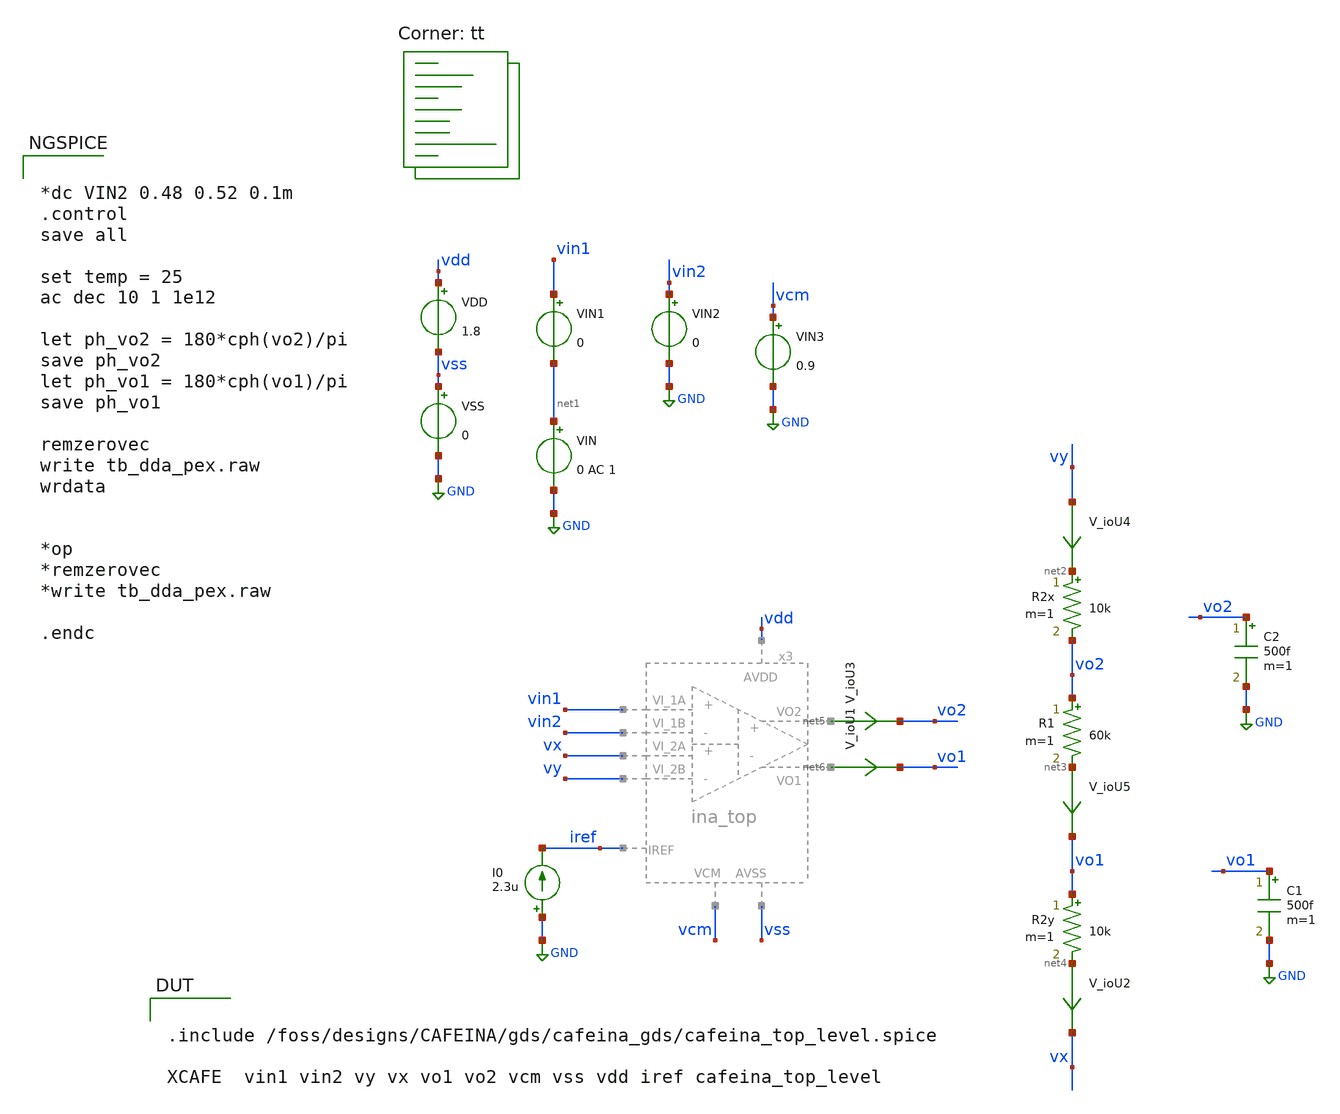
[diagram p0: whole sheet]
** sch_path: xschem/testbenches/tb_dda_pex.sch
**.subckt tb_dda_pex
VDD vdd vss 1.8
VSS vss GND 0
C1 vo1 GND 500f m=1
I0 GND iref 2.3u
VIN1 vin1 net1 0
VIN2 vin2 GND 0
VIN net1 GND 0 AC 1
C2 vo2 GND 500f m=1
VIN3 vcm GND 0.9
R2x net2 vo2 10k m=1
R1 vo2 net3 60k m=1
R2y vo1 net4 10k m=1
V_ioU3 net5 vo2 0
.save i(v_iou3)
V_ioU1 net6 vo1 0
.save i(v_iou1)
V_ioU2 net4 vx 0
.save i(v_iou2)
V_ioU4 vy net2 0
.save i(v_iou4)
V_ioU5 net3 vo1 0
.save i(v_iou5)
**** begin user architecture code


*dc VIN2 0.48 0.52 0.1m
.control
save all

set temp = 25
ac dec 10 1 1e12

let ph_vo2 = 180*cph(vo2)/pi
save ph_vo2
let ph_vo1 = 180*cph(vo1)/pi
save ph_vo1

remzerovec
write tb_dda_pex.raw
wrdata


*op
*remzerovec
*write tb_dda_pex.raw

.endc


.lib $::SKYWATER_MODELS/sky130.lib.spice tt


.include /foss/designs/CAFEINA/gds/cafeina_gds/cafeina_top_level.spice

XCAFE  vin1 vin2 vy vx vo1 vo2 vcm vss vdd iref cafeina_top_level



**** end user architecture code
**.ends
.GLOBAL GND
.end
